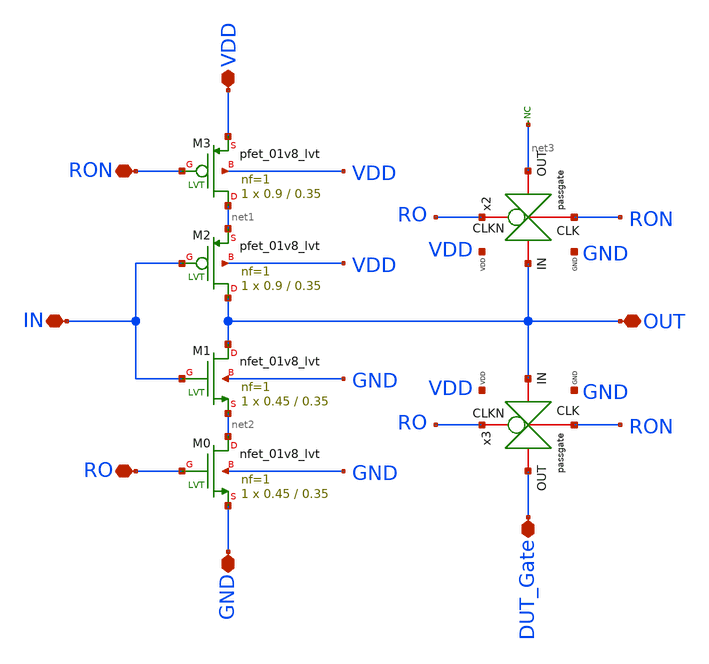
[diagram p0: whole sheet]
** sch_path: LVT/rovcel3_LVT/rovcel3_LVT.sch
**.subckt rovcel3_LVT OUT DUT_Gate RON RO IN VDD GND
*.iopin OUT
*.iopin DUT_Gate
*.iopin RON
*.iopin RO
*.iopin IN
*.iopin VDD
*.iopin GND
XM0 net2 RO GND GND sky130_fd_pr__nfet_01v8_lvt L=0.35 W=0.45 nf=1 ad='int((nf+1)/2) * W/nf * 0.29' as='int((nf+2)/2) * W/nf * 0.29'
+ pd='2*int((nf+1)/2) * (W/nf + 0.29)' ps='2*int((nf+2)/2) * (W/nf + 0.29)' nrd='0.29 / W' nrs='0.29 / W'
+ sa=0 sb=0 sd=0 mult=1 m=1
XM1 OUT IN net2 GND sky130_fd_pr__nfet_01v8_lvt L=0.35 W=0.45 nf=1 ad='int((nf+1)/2) * W/nf * 0.29' as='int((nf+2)/2) * W/nf * 0.29'
+ pd='2*int((nf+1)/2) * (W/nf + 0.29)' ps='2*int((nf+2)/2) * (W/nf + 0.29)' nrd='0.29 / W' nrs='0.29 / W'
+ sa=0 sb=0 sd=0 mult=1 m=1
XM2 OUT IN net1 VDD sky130_fd_pr__pfet_01v8_lvt L=0.35 W=0.9 nf=1 ad='int((nf+1)/2) * W/nf * 0.29' as='int((nf+2)/2) * W/nf * 0.29'
+ pd='2*int((nf+1)/2) * (W/nf + 0.29)' ps='2*int((nf+2)/2) * (W/nf + 0.29)' nrd='0.29 / W' nrs='0.29 / W'
+ sa=0 sb=0 sd=0 mult=1 m=1
XM3 net1 RON VDD VDD sky130_fd_pr__pfet_01v8_lvt L=0.35 W=0.9 nf=1 ad='int((nf+1)/2) * W/nf * 0.29' as='int((nf+2)/2) * W/nf * 0.29'
+ pd='2*int((nf+1)/2) * (W/nf + 0.29)' ps='2*int((nf+2)/2) * (W/nf + 0.29)' nrd='0.29 / W' nrs='0.29 / W'
+ sa=0 sb=0 sd=0 mult=1 m=1
* noconn #net3
x2 RO OUT net3 RON GND VDD passgate
x3 RO OUT DUT_Gate RON GND VDD passgate
**.ends
.end
